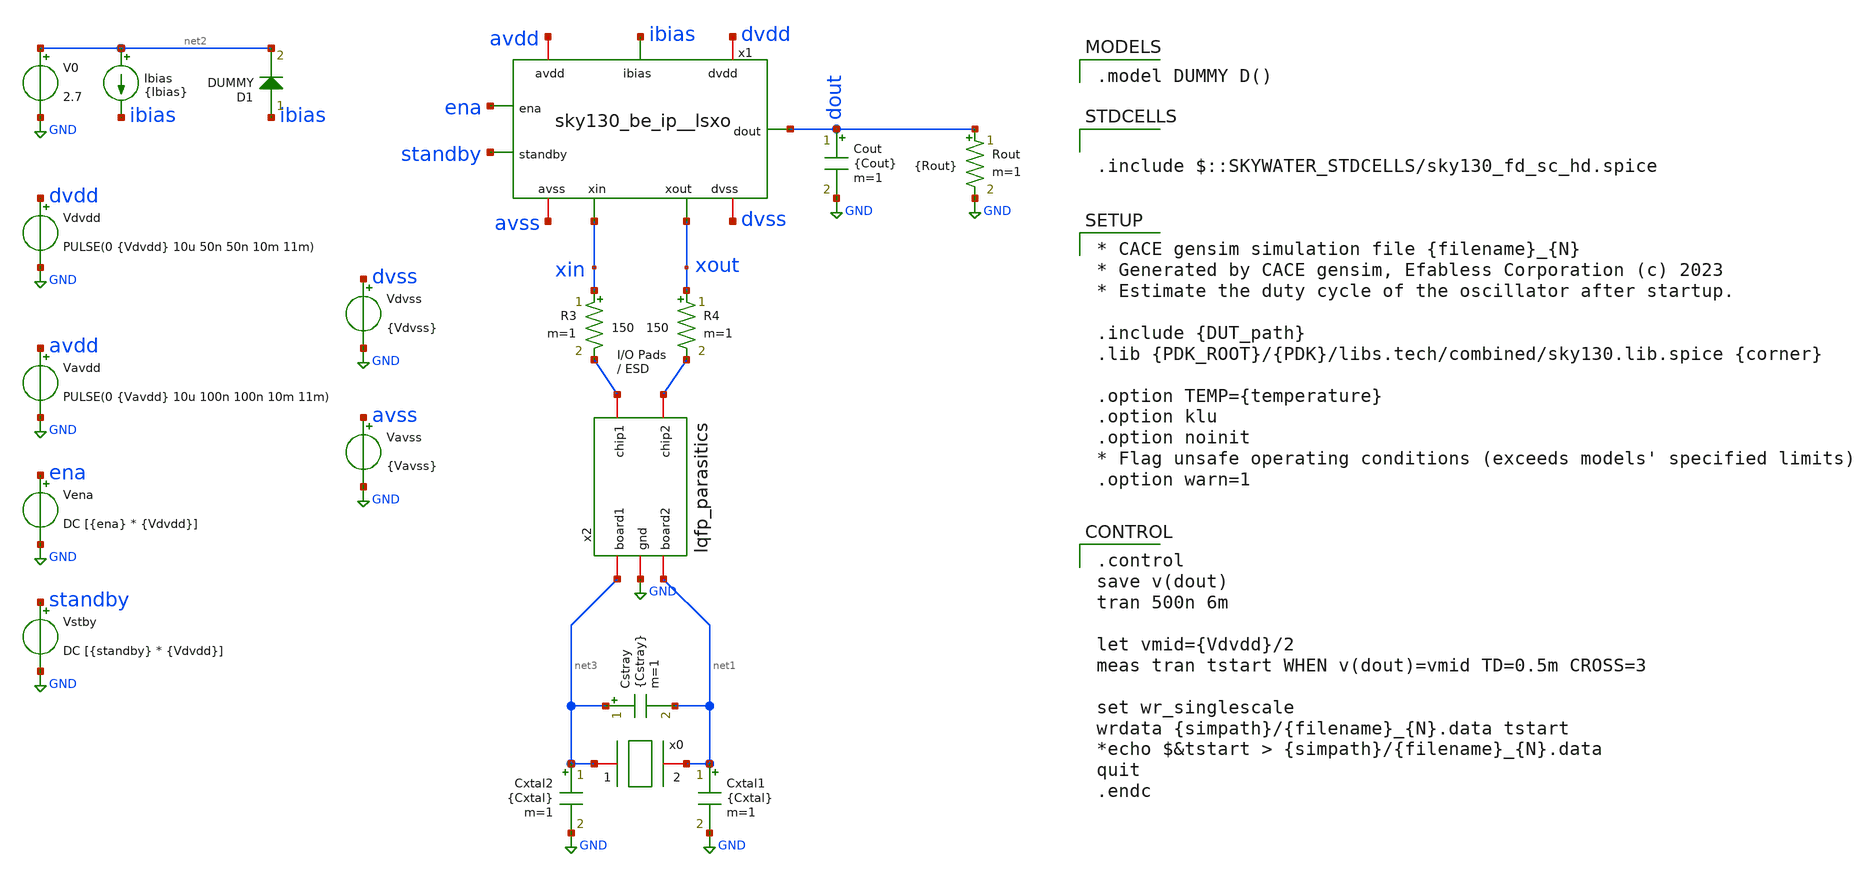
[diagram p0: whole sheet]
** sch_path: cace/templates/tb_startup_pwron.sch

.include $::SKYWATER_STDCELLS/sky130_fd_sc_hd.spice

**.subckt tb_startup_pwron
Vdvdd dvdd GND PULSE(0 {Vdvdd} 10u 50n 50n 10m 11m)
Vavdd avdd GND PULSE(0 {Vavdd} 10u 100n 100n 10m 11m)
Cxtal2 net3 GND {Cxtal} m=1
Cxtal1 net1 GND {Cxtal} m=1
Cstray net3 net1 {Cstray} m=1
Ibias net2 ibias {Ibias}
Cout dout GND {Cout} m=1
V0 net2 GND 2.7
R3 xin net4 150 m=1
R4 xout net5 150 m=1
x2 net5 net4 GND net3 net1 lqfp_parasitics
D1 ibias net2 DUMMY area=100
x1 avdd avss dvdd dvss ibias ena standby dout xin xout sky130_be_ip__lsxo
Vdvss dvss GND {Vdvss}
Vavss avss GND {Vavss}
Rout dout GND {Rout} m=1
x0 net3 net1 xtal_iqd_125_1
Vena ena GND DC [{ena} * {Vdvdd}]
Vstby standby GND DC [{standby} * {Vdvdd}]
**** begin user architecture code

.model DUMMY D()


.control
save v(dout)
tran 500n 6m

let vmid={Vdvdd}/2
meas tran tstart WHEN v(dout)=vmid TD=0.5m CROSS=3

set wr_singlescale
wrdata {simpath}/{filename}_{N}.data tstart
*echo $&tstart > {simpath}/{filename}_{N}.data
quit
.endc



* CACE gensim simulation file {filename}_{N}
* Generated by CACE gensim, Efabless Corporation (c) 2023
* Estimate the duty cycle of the oscillator after startup.

.include {DUT_path}
.lib {PDK_ROOT}/{PDK}/libs.tech/combined/sky130.lib.spice {corner}

.option TEMP={temperature}
.option klu
.option noinit
* Flag unsafe operating conditions (exceeds models' specified limits)
.option warn=1


**** end user architecture code
**.ends
.GLOBAL GND
.end
